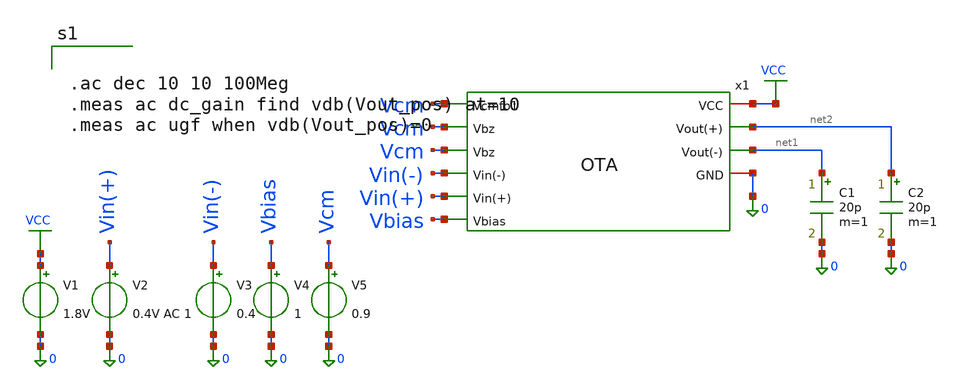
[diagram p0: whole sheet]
** sch_path: blocks/01_OTA/sim/tb_OTA_AC.sch
**.subckt tb_OTA_AC
x1 VCC Vcm Vcm Vin(-) Vin(+) net2 net1 Vbias 0 OTA
V1 VCC 0 1.8V
V2 Vin(+) 0 0.4V AC 1
V3 Vin(-) 0 0.4
V4 Vbias 0 1
V5 Vcm 0 0.9
C1 net1 0 20p m=1
C2 net2 0 20p m=1
**** begin user architecture code


.ac dec 10 10 100Meg
.meas ac dc_gain find vdb(Vout_pos) at=10
.meas ac ugf when vdb(Vout_pos)=0


**** end user architecture code
**.ends

* expanding   symbol:  blocks/01_OTA/xschem/OTA.sym # of pins=10
** sym_path: blocks/01_OTA/xschem/OTA.sym
** sch_path: blocks/01_OTA/xschem/OTA.sch
.subckt OTA VCC Vcmfb1 Vbz Vin(-) Vin(+) Vout(+) Vout(-) Vbias GND
*.ipin Vin(+)
*.ipin Vin(-)
*.ipin Vbias
*.ipin Vbz
*.ipin Vbz
*.ipin Vcmfb1
*.opin Vout(+)
*.opin Vout(-)
*.iopin VCC
*.iopin GND
XM1 net5 Vin(+) net3 net5 sky130_fd_pr__pfet_01v8 L=0.15 W=1 nf=1 ad='int((1 + 1)/2) * 1 / 1 * 0.29'
+ as='int((1 + 2)/2) * 1 / 1 * 0.29' pd='2*int((1 + 1)/2) * (1 / 1 + 0.29)' ps='2*int((1 + 2)/2) * (1 / 1 + 0.29)'
+ nrd='0.29 / 1 ' nrs='0.29 / 1 ' sa=0 sb=0 sd=0 mult=1 m=1
XM2 net5 Vin(-) net4 net5 sky130_fd_pr__pfet_01v8 L=0.15 W=1 nf=1 ad='int((1 + 1)/2) * 1 / 1 * 0.29'
+ as='int((1 + 2)/2) * 1 / 1 * 0.29' pd='2*int((1 + 1)/2) * (1 / 1 + 0.29)' ps='2*int((1 + 2)/2) * (1 / 1 + 0.29)'
+ nrd='0.29 / 1 ' nrs='0.29 / 1 ' sa=0 sb=0 sd=0 mult=1 m=1
XM3 net3 Vbias GND GND sky130_fd_pr__nfet_01v8 L=0.15 W=1 nf=1 ad='int((1 + 1)/2) * 1 / 1 * 0.29' as='int((1 + 2)/2) * 1 / 1 * 0.29'
+ pd='2*int((1 + 1)/2) * (1 / 1 + 0.29)' ps='2*int((1 + 2)/2) * (1 / 1 + 0.29)' nrd='0.29 / 1 ' nrs='0.29 / 1 '
+ sa=0 sb=0 sd=0 mult=1 m=1
XM4 net4 Vbias GND GND sky130_fd_pr__nfet_01v8 L=0.15 W=1 nf=1 ad='int((1 + 1)/2) * 1 / 1 * 0.29' as='int((1 + 2)/2) * 1 / 1 * 0.29'
+ pd='2*int((1 + 1)/2) * (1 / 1 + 0.29)' ps='2*int((1 + 2)/2) * (1 / 1 + 0.29)' nrd='0.29 / 1 ' nrs='0.29 / 1 '
+ sa=0 sb=0 sd=0 mult=1 m=1
XM5 net1 net4 GND GND sky130_fd_pr__nfet_01v8 L=0.15 W=1 nf=1 ad='int((1 + 1)/2) * 1 / 1 * 0.29' as='int((1 + 2)/2) * 1 / 1 * 0.29'
+ pd='2*int((1 + 1)/2) * (1 / 1 + 0.29)' ps='2*int((1 + 2)/2) * (1 / 1 + 0.29)' nrd='0.29 / 1 ' nrs='0.29 / 1 '
+ sa=0 sb=0 sd=0 mult=1 m=1
XM6 net2 net3 GND GND sky130_fd_pr__nfet_01v8 L=0.15 W=1 nf=1 ad='int((1 + 1)/2) * 1 / 1 * 0.29' as='int((1 + 2)/2) * 1 / 1 * 0.29'
+ pd='2*int((1 + 1)/2) * (1 / 1 + 0.29)' ps='2*int((1 + 2)/2) * (1 / 1 + 0.29)' nrd='0.29 / 1 ' nrs='0.29 / 1 '
+ sa=0 sb=0 sd=0 mult=1 m=1
XM7 VCC net1 net1 VCC sky130_fd_pr__pfet_01v8 L=0.15 W=1 nf=1 ad='int((1 + 1)/2) * 1 / 1 * 0.29' as='int((1 + 2)/2) * 1 / 1 * 0.29'
+ pd='2*int((1 + 1)/2) * (1 / 1 + 0.29)' ps='2*int((1 + 2)/2) * (1 / 1 + 0.29)' nrd='0.29 / 1 ' nrs='0.29 / 1 '
+ sa=0 sb=0 sd=0 mult=1 m=1
XM8 VCC net2 net2 VCC sky130_fd_pr__pfet_01v8 L=0.15 W=1 nf=1 ad='int((1 + 1)/2) * 1 / 1 * 0.29' as='int((1 + 2)/2) * 1 / 1 * 0.29'
+ pd='2*int((1 + 1)/2) * (1 / 1 + 0.29)' ps='2*int((1 + 2)/2) * (1 / 1 + 0.29)' nrd='0.29 / 1 ' nrs='0.29 / 1 '
+ sa=0 sb=0 sd=0 mult=1 m=1
XM9 VCC net1 Vout(+) VCC sky130_fd_pr__pfet_01v8 L=0.15 W=1 nf=1 ad='int((1 + 1)/2) * 1 / 1 * 0.29' as='int((1 + 2)/2) * 1 / 1 * 0.29'
+ pd='2*int((1 + 1)/2) * (1 / 1 + 0.29)' ps='2*int((1 + 2)/2) * (1 / 1 + 0.29)' nrd='0.29 / 1 ' nrs='0.29 / 1 '
+ sa=0 sb=0 sd=0 mult=1 m=1
XM10 VCC net2 Vout(-) VCC sky130_fd_pr__pfet_01v8 L=0.15 W=1 nf=1 ad='int((1 + 1)/2) * 1 / 1 * 0.29'
+ as='int((1 + 2)/2) * 1 / 1 * 0.29' pd='2*int((1 + 1)/2) * (1 / 1 + 0.29)' ps='2*int((1 + 2)/2) * (1 / 1 + 0.29)'
+ nrd='0.29 / 1 ' nrs='0.29 / 1 ' sa=0 sb=0 sd=0 mult=1 m=1
XM11 Vout(+) net8 GND GND sky130_fd_pr__nfet_01v8 L=0.15 W=1 nf=1 ad='int((1 + 1)/2) * 1 / 1 * 0.29'
+ as='int((1 + 2)/2) * 1 / 1 * 0.29' pd='2*int((1 + 1)/2) * (1 / 1 + 0.29)' ps='2*int((1 + 2)/2) * (1 / 1 + 0.29)'
+ nrd='0.29 / 1 ' nrs='0.29 / 1 ' sa=0 sb=0 sd=0 mult=1 m=1
XM12 Vout(-) net9 GND GND sky130_fd_pr__nfet_01v8 L=0.15 W=1 nf=1 ad='int((1 + 1)/2) * 1 / 1 * 0.29'
+ as='int((1 + 2)/2) * 1 / 1 * 0.29' pd='2*int((1 + 1)/2) * (1 / 1 + 0.29)' ps='2*int((1 + 2)/2) * (1 / 1 + 0.29)'
+ nrd='0.29 / 1 ' nrs='0.29 / 1 ' sa=0 sb=0 sd=0 mult=1 m=1
XM13 VCC Vcmfb1 net5 VCC sky130_fd_pr__pfet_01v8 L=0.15 W=1 nf=1 ad='int((1 + 1)/2) * 1 / 1 * 0.29' as='int((1 + 2)/2) * 1 / 1 * 0.29'
+ pd='2*int((1 + 1)/2) * (1 / 1 + 0.29)' ps='2*int((1 + 2)/2) * (1 / 1 + 0.29)' nrd='0.29 / 1 ' nrs='0.29 / 1 '
+ sa=0 sb=0 sd=0 mult=1 m=1
XC1 Vout(+) net6 sky130_fd_pr__cap_mim_m3_1 W=1 L=1 MF=1 m=1
XMbz1 net6 Vbz net8 GND sky130_fd_pr__nfet_01v8 L=0.15 W=1 nf=1 ad='int((1 + 1)/2) * 1 / 1 * 0.29' as='int((1 + 2)/2) * 1 / 1 * 0.29'
+ pd='2*int((1 + 1)/2) * (1 / 1 + 0.29)' ps='2*int((1 + 2)/2) * (1 / 1 + 0.29)' nrd='0.29 / 1 ' nrs='0.29 / 1 '
+ sa=0 sb=0 sd=0 mult=1 m=1
XC2 net7 Vout(-) sky130_fd_pr__cap_mim_m3_1 W=1 L=1 MF=1 m=1
XM14 net9 Vbz net7 GND sky130_fd_pr__nfet_01v8 L=0.15 W=1 nf=1 ad='int((1 + 1)/2) * 1 / 1 * 0.29' as='int((1 + 2)/2) * 1 / 1 * 0.29'
+ pd='2*int((1 + 1)/2) * (1 / 1 + 0.29)' ps='2*int((1 + 2)/2) * (1 / 1 + 0.29)' nrd='0.29 / 1 ' nrs='0.29 / 1 '
+ sa=0 sb=0 sd=0 mult=1 m=1
.ends

.GLOBAL VCC
.end
